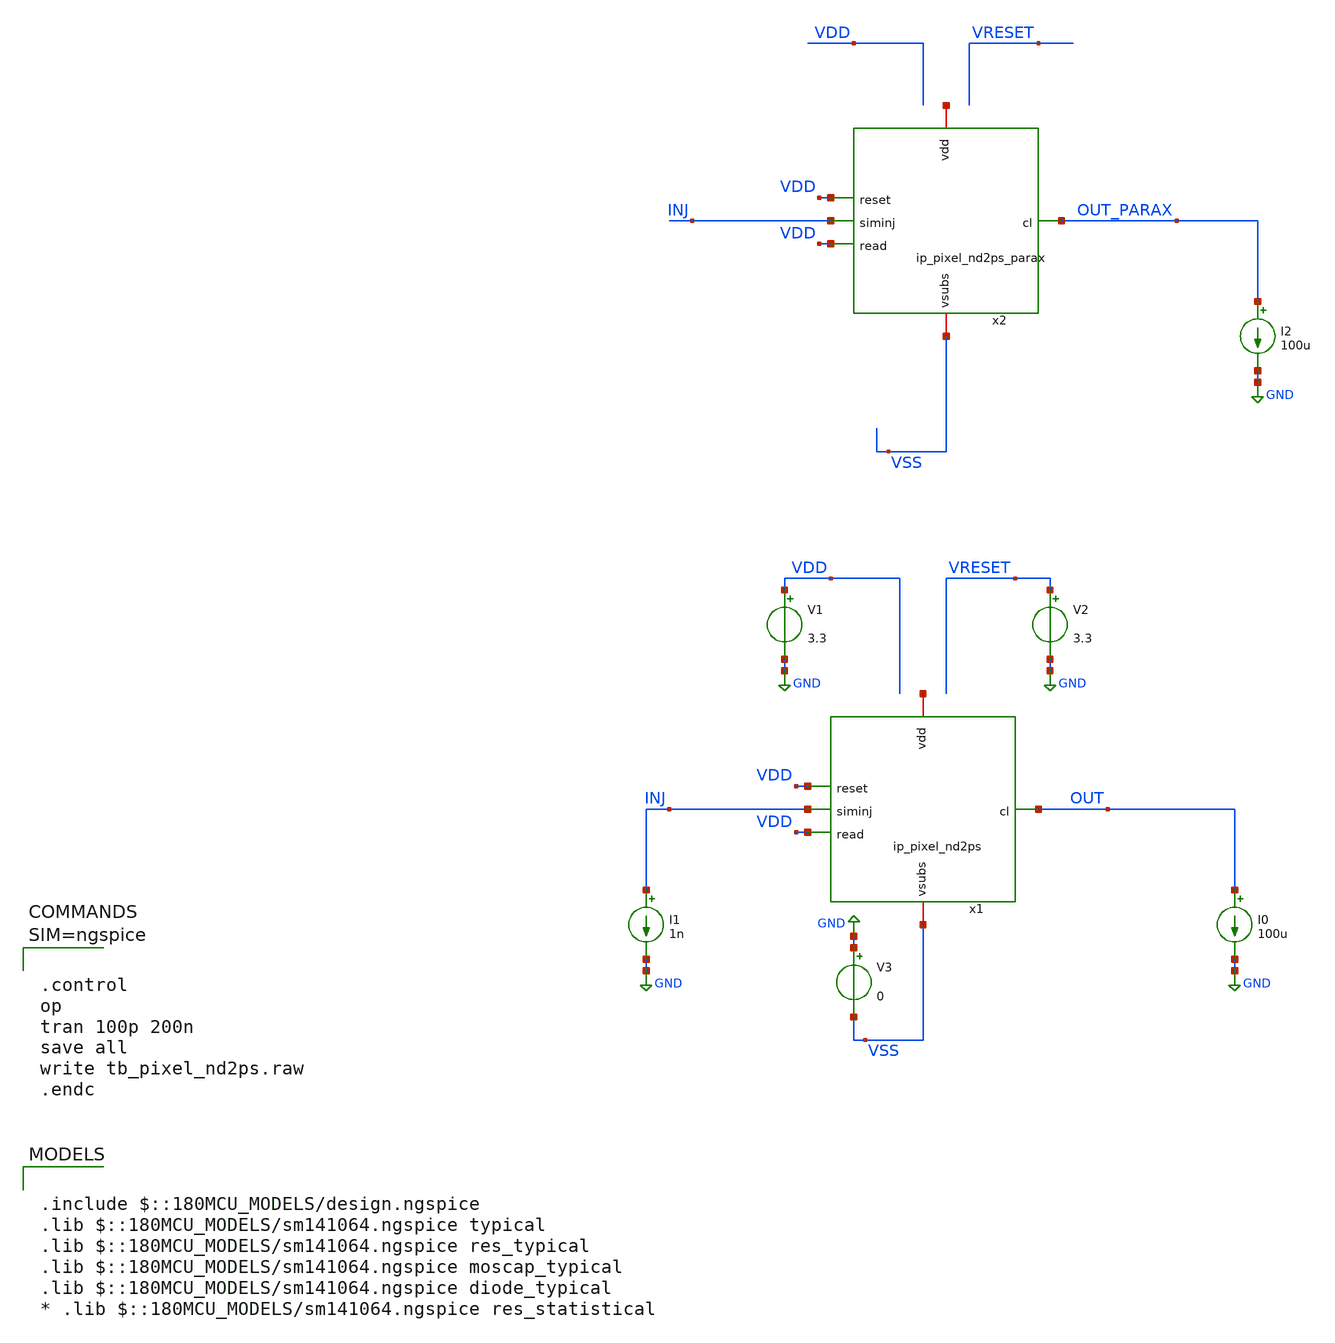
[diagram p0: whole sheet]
** sch_path: xschem/tb_pixel_nd2ps.sch
**.subckt tb_pixel_nd2ps
V1 VDD GND 3.3
V2 VRESET GND 3.3
V3 GND VSS 0
I0 OUT GND 100u
I1 INJ GND 1n
x1 net1 VDD INJ VDD VSS OUT ip_pixel_nd2ps
I2 OUT_PARAX GND 100u
x2 net2 VDD INJ VDD VSS OUT_PARAX ip_pixel_nd2ps_parax
**** begin user architecture code

.include $::180MCU_MODELS/design.ngspice
.lib $::180MCU_MODELS/sm141064.ngspice typical
.lib $::180MCU_MODELS/sm141064.ngspice res_typical
.lib $::180MCU_MODELS/sm141064.ngspice moscap_typical
.lib $::180MCU_MODELS/sm141064.ngspice diode_typical
* .lib $::180MCU_MODELS/sm141064.ngspice res_statistical




.control
op
tran 100p 200n
save all
write tb_pixel_nd2ps.raw
.endc



**** end user architecture code
**.ends

* expanding   symbol:  ip_pixel_nd2ps.sym # of pins=6
** sym_path: xschem/ip_pixel_nd2ps.sym
** sch_path: xschem/ip_pixel_nd2ps.sch
.subckt ip_pixel_nd2ps vdd reset siminj read vsubs cl
*.iopin vdd
*.iopin vsubs
*.ipin siminj
*.ipin reset
*.ipin read
*.opin cl
XM1 vdd reset siminj vsubs nfet_03v3 L=0.3u W=0.3u nf=1 ad='int((nf+1)/2) * W/nf * 0.18u' as='int((nf+2)/2) * W/nf * 0.18u'
+ pd='2*int((nf+1)/2) * (W/nf + 0.18u)' ps='2*int((nf+2)/2) * (W/nf + 0.18u)' nrd='0.18u / W' nrs='0.18u / W'
+ sa=0 sb=0 sd=0 m=1
XM2 vdd siminj sfout vsubs nfet_03v3 L=1u W=2.5u nf=1 ad='int((nf+1)/2) * W/nf * 0.18u' as='int((nf+2)/2) * W/nf * 0.18u'
+ pd='2*int((nf+1)/2) * (W/nf + 0.18u)' ps='2*int((nf+2)/2) * (W/nf + 0.18u)' nrd='0.18u / W' nrs='0.18u / W'
+ sa=0 sb=0 sd=0 m=1
XM3 sfout read cl vsubs nfet_03v3 L=0.3u W=0.3u nf=1 ad='int((nf+1)/2) * W/nf * 0.18u' as='int((nf+2)/2) * W/nf * 0.18u'
+ pd='2*int((nf+1)/2) * (W/nf + 0.18u)' ps='2*int((nf+2)/2) * (W/nf + 0.18u)' nrd='0.18u / W' nrs='0.18u / W'
+ sa=0 sb=0 sd=0 m=1
D1 vsubs siminj diode_nd2ps_03v3 area='13.5u * 13.5u ' pj='2*13.5u + 2*13.5u ' m=1
.ends


* expanding   symbol:  ip_pixel_nd2ps_parax.sym # of pins=6
** sym_path: xschem/ip_pixel_nd2ps.sym
.include [file normalize ../mag/ip_pixel_nd2ps.sim.spice]
.GLOBAL GND
.end
